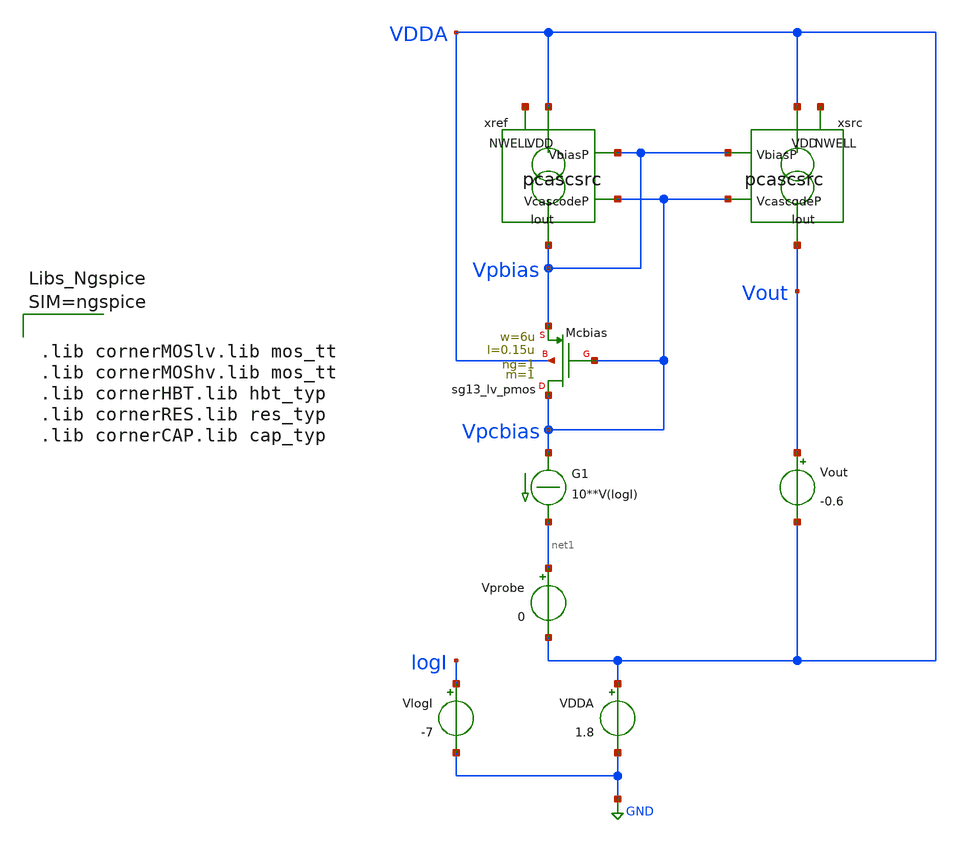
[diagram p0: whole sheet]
** sch_path: xschem/test_pcascsrc_DC.sch
**.subckt test_pcascsrc_DC
Vout Vout VDDA -0.6
.save i(vout)
Vprobe net1 VDDA 0
.save i(vprobe)
G1 Vpcbias net1 CUR=' 10**V(logI) '
VlogI logI GND -7
.save i(vlogi)
xref VDDA Vpbias Vpcbias Vpbias net2 pcascsrc
xsrc VDDA Vpbias Vpcbias Vout net3 pcascsrc
VDDA VDDA GND 1.8
.save i(vdda)
XMcbias Vpcbias Vpcbias Vpbias VDDA sg13_lv_pmos w=6u l=0.15u ng=1 m=1 mm_ok=1
**** begin user architecture code


.include test_pcascsrc_DC.save
.param temp=27
.options savecurrents
.control
save all
op
write test_pcascsrc_DC.raw
set appendwrite
dc Vout 0 -1.8 -10m VlogI -8 -6 0.5
write test_pcascsrc_DC.raw
plot 2*(vout#branch-vprobe#branch)/(vprobe#branch+vout#branch)
plot vdda vpbias vpcbias vout xref.drain xsrc.drain
plot @n.xref.xmsrc.nsg13_lv_pmos[gm]/vprobe#branch @n.xref.xmcasc.nsg13_lv_pmos[gm]/vprobe#branch
+ @n.xsrc.xmsrc.nsg13_lv_pmos[gm]/vout#branch @n.xsrc.xmcasc.nsg13_lv_pmos[gm]/vout#branch
plot @n.xref.xmsrc.nsg13_lv_pmos[gm]/@n.xref.xmsrc.nsg13_lv_pmos[gds]
+ @n.xref.xmcasc.nsg13_lv_pmos[gm]/@n.xref.xmcasc.nsg13_lv_pmos[gds] @n.xsrc.xmsrc.nsg13_lv_pmos[gm]/@n.xsrc.xmsrc.nsg13_lv_pmos[gds]
+ @n.xsrc.xmcasc.nsg13_lv_pmos[gm]/@n.xsrc.xmcasc.nsg13_lv_pmos[gds]
plot @n.xref.xmsrc.nsg13_lv_pmos[vth] @n.xref.xmcasc.nsg13_lv_pmos[vth]
+ @n.xsrc.xmsrc.nsg13_lv_pmos[vth] @n.xsrc.xmcasc.nsg13_lv_pmos[vth]
.endc





.lib cornerMOSlv.lib mos_tt
.lib cornerMOShv.lib mos_tt
.lib cornerHBT.lib hbt_typ
.lib cornerRES.lib res_typ
.lib cornerCAP.lib cap_typ



**** end user architecture code
**.ends

* expanding   symbol:  pcascsrc.sym # of pins=5
** sym_path: xschem/pcascsrc.sym
** sch_path: xschem/pcascsrc.sch
.subckt pcascsrc VDD VbiasP VcascodeP Iout NWELL
*.ipin VcascodeP
*.ipin VbiasP
*.opin Iout
*.ipin VDD
*.iopin NWELL
XMsrc drain VbiasP VDD NWELL sg13_lv_pmos w=0.74u l=2u ng=1 m=1 mm_ok=1
XMcasc Iout VcascodeP drain NWELL sg13_lv_pmos w=0.3u l=0.3u ng=1 m=1 mm_ok=1
.ends

.GLOBAL GND
.end
